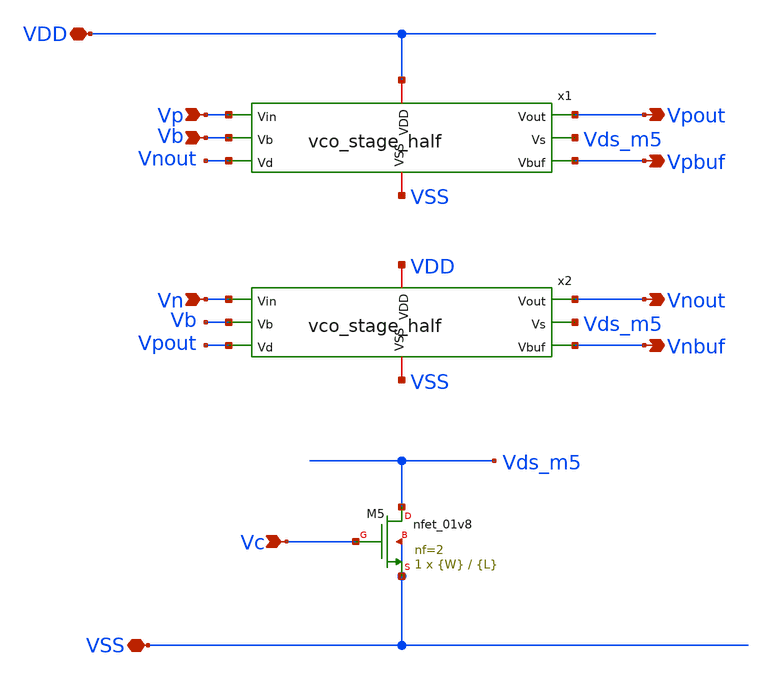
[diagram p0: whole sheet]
** sch_path: xschem/vco_stage_p.sch
**.subckt vco_stage_p VDD VSS Vp Vn Vb Vc Vpout Vnout Vpbuf Vnbuf
*.iopin VDD
*.iopin VSS
*.ipin Vp
*.ipin Vn
*.ipin Vb
*.ipin Vc
*.opin Vpout
*.opin Vnout
*.opin Vpbuf
*.opin Vnbuf
x1 VDD VSS Vp Vb Vnout Vpout Vds_m5 Vpbuf vco_stage_half
x2 VDD VSS Vn Vb Vpout Vnout Vds_m5 Vnbuf vco_stage_half
XM5 Vds_m5 Vc VSS VSS sky130_fd_pr__nfet_01v8 L={L} W={W} nf=2 ad='int((nf+1)/2) * W/nf * 0.29' as='int((nf+2)/2) * W/nf * 0.29'
+ pd='2*int((nf+1)/2) * (W/nf + 0.29)' ps='2*int((nf+2)/2) * (W/nf + 0.29)' nrd='0.29 / W' nrs='0.29 / W'
+ sa=0 sb=0 sd=0 mult=1 m=1
**.ends
.end
